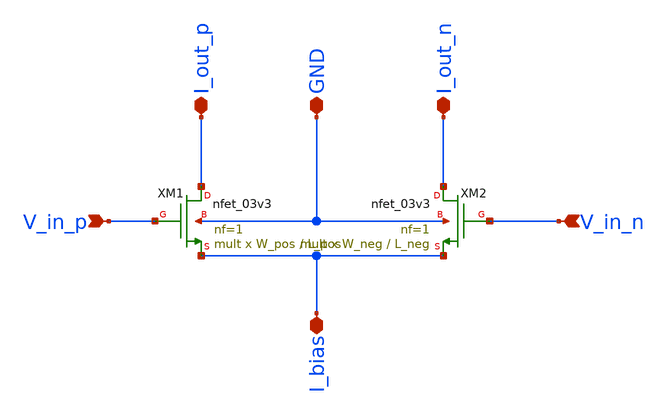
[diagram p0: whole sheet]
** sch_path: src/design_xsch/experimental_hierarchal/diff_pair.sch
**.subckt diff_pair V_in_p V_in_n I_out_p I_out_n I_bias GND
*.ipin V_in_p
*.ipin V_in_n
*.iopin I_out_p
*.iopin I_out_n
*.iopin I_bias
*.iopin GND
XM1 I_out_p V_in_p I_bias GND nfet_03v3 L=L_pos W=W_pos nf=1 ad='int((nf+1)/2) * W/nf * 0.18u' as='int((nf+2)/2) * W/nf * 0.18u'
+ pd='2*int((nf+1)/2) * (W/nf + 0.18u)' ps='2*int((nf+2)/2) * (W/nf + 0.18u)' nrd='0.18u / W' nrs='0.18u / W'
+ sa=0 sb=0 sd=0 m=mult
XM2 I_out_n V_in_n I_bias GND nfet_03v3 L=L_neg W=W_neg nf=1 ad='int((nf+1)/2) * W/nf * 0.18u' as='int((nf+2)/2) * W/nf * 0.18u'
+ pd='2*int((nf+1)/2) * (W/nf + 0.18u)' ps='2*int((nf+2)/2) * (W/nf + 0.18u)' nrd='0.18u / W' nrs='0.18u / W'
+ sa=0 sb=0 sd=0 m=mult
**.ends
.end
